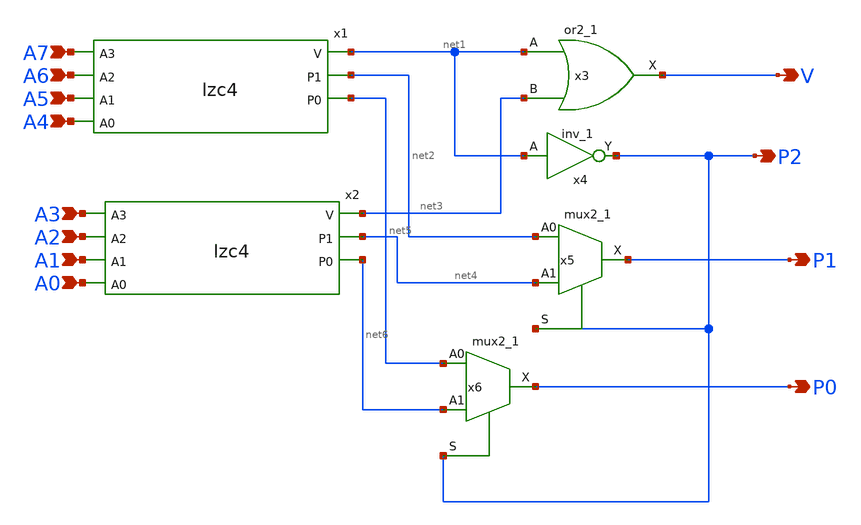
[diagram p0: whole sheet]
** sch_path: frontend/xschem/lzc8.sch
**.subckt lzc8 A7 A6 A5 A4 A3 A2 A1 A0 V P2 P1 P0
*.ipin A7
*.ipin A6
*.ipin A5
*.ipin A4
*.ipin A3
*.ipin A2
*.ipin A1
*.ipin A0
*.opin V
*.opin P2
*.opin P1
*.opin P0
x1 A7 net1 A6 net2 A5 A4 net5 lzc4
x2 A3 net3 A2 net4 A1 A0 net6 lzc4
x3 net1 net3 VGND VNB VPB VPWR V sky130_fd_sc_hd__or2_1
x4 net1 VGND VNB VPB VPWR P2 sky130_fd_sc_hd__inv_1
x5 net2 net4 P2 VGND VNB VPB VPWR P1 sky130_fd_sc_hd__mux2_1
x6 net5 net6 P2 VGND VNB VPB VPWR P0 sky130_fd_sc_hd__mux2_1
**.ends

* expanding   symbol:  lzc4.sym # of pins=7
** sym_path: frontend/xschem/lzc4.sym
** sch_path: frontend/xschem/lzc4.sch
.subckt lzc4 A3 V A2 P1 A1 A0 P0
*.ipin A3
*.ipin A2
*.ipin A1
*.ipin A0
*.opin V
*.opin P1
*.opin P0
x1 A3 net1 A2 net3 lzc2
x2 A1 net2 A0 net4 lzc2
x3 net1 net2 VGND VNB VPB VPWR V sky130_fd_sc_hd__or2_1
x4 net1 VGND VNB VPB VPWR P1 sky130_fd_sc_hd__inv_1
x5 net3 net4 P1 VGND VNB VPB VPWR P0 sky130_fd_sc_hd__mux2_1
.ends


* expanding   symbol:  lzc2.sym # of pins=4
** sym_path: frontend/xschem/lzc2.sym
** sch_path: frontend/xschem/lzc2.sch
.subckt lzc2 HI V LO P
*.ipin HI
*.ipin LO
*.opin V
*.opin P
x1 HI LO VGND VNB VPB VPWR V sky130_fd_sc_hd__or2_1
x2 HI GND GND VDD VDD P sky130_fd_sc_hd__inv_1
.ends

.end
